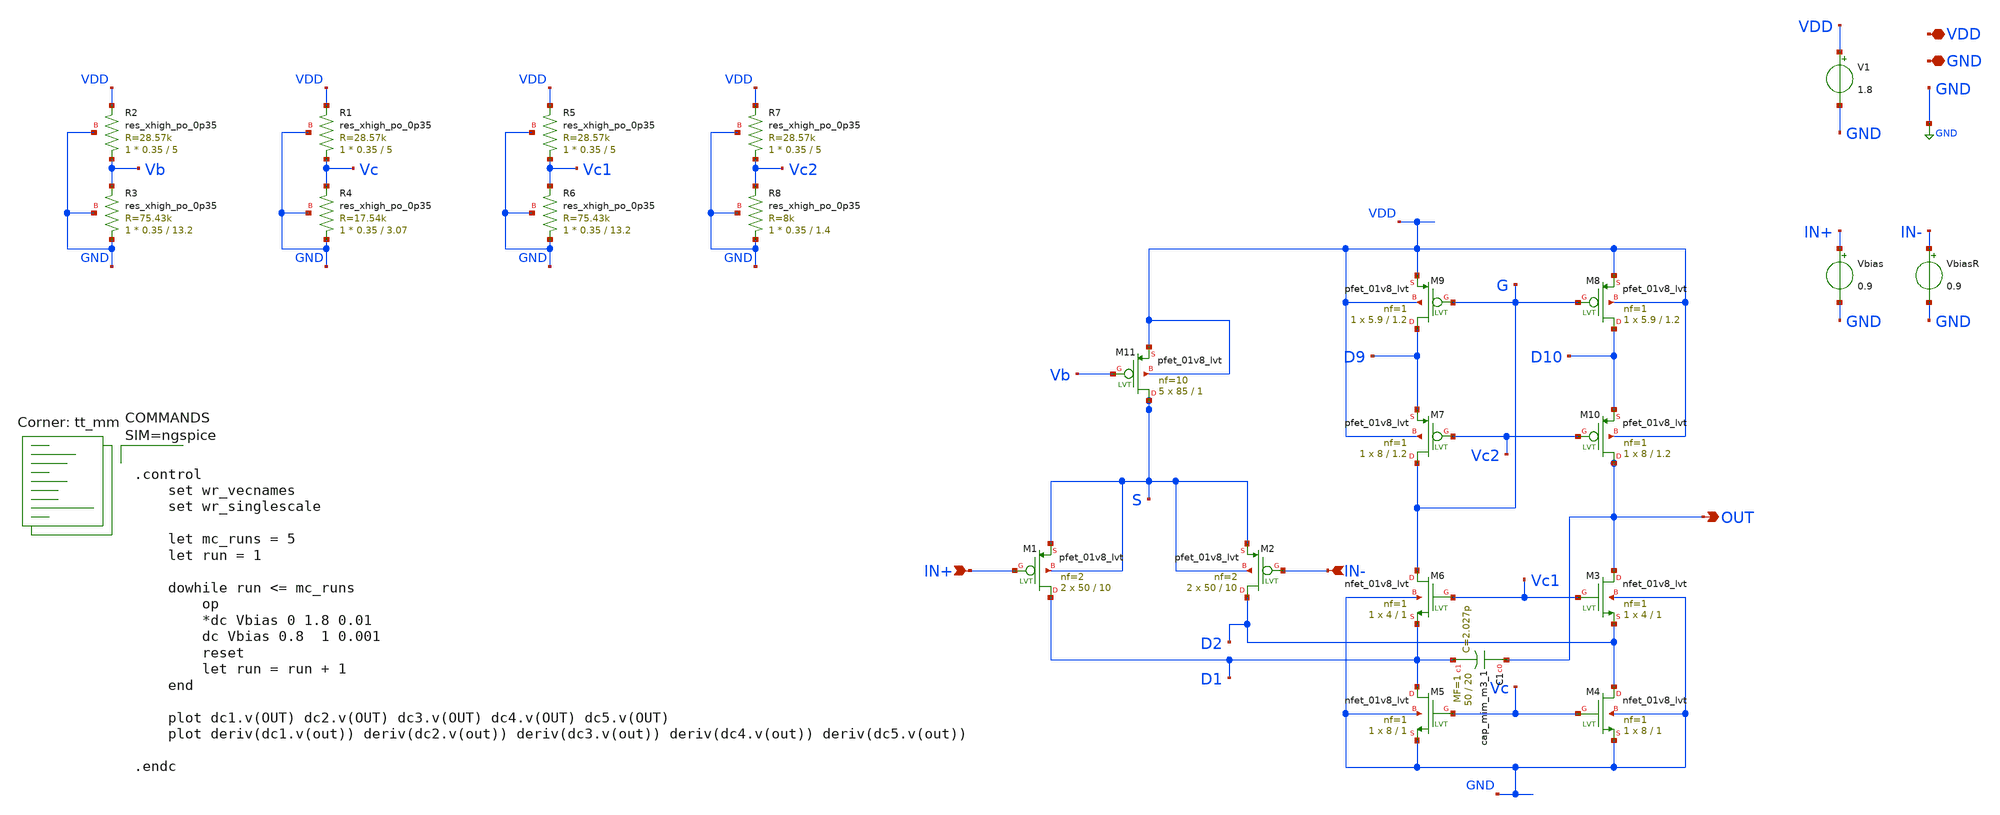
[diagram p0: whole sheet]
** sch_path: xschem/OTA_FoldedCascode1_1_MC.sch
**.subckt OTA_FoldedCascode1_1_MC VDD GND IN+ IN- OUT
*.iopin VDD
*.iopin GND
*.ipin IN+
*.ipin IN-
*.opin OUT
V1 VDD GND 1.8
Vbias IN+ GND 0.9
VbiasR IN- GND 0.9
XM11 S Vb VDD VDD sky130_fd_pr__pfet_01v8_lvt L=1 W=85 nf=10 ad='int((nf+1)/2) * W/nf * 0.29' as='int((nf+2)/2) * W/nf * 0.29'
+ pd='2*int((nf+1)/2) * (W/nf + 0.29)' ps='2*int((nf+2)/2) * (W/nf + 0.29)' nrd='0.29 / W' nrs='0.29 / W'
+ sa=0 sb=0 sd=0 mult=5 m=5
XM1 D1 IN+ S S sky130_fd_pr__pfet_01v8_lvt L=10 W=50 nf=2 ad='int((nf+1)/2) * W/nf * 0.29' as='int((nf+2)/2) * W/nf * 0.29'
+ pd='2*int((nf+1)/2) * (W/nf + 0.29)' ps='2*int((nf+2)/2) * (W/nf + 0.29)' nrd='0.29 / W' nrs='0.29 / W'
+ sa=0 sb=0 sd=0 mult=2 m=2
XM2 D2 IN- S S sky130_fd_pr__pfet_01v8_lvt L=10 W=50 nf=2 ad='int((nf+1)/2) * W/nf * 0.29' as='int((nf+2)/2) * W/nf * 0.29'
+ pd='2*int((nf+1)/2) * (W/nf + 0.29)' ps='2*int((nf+2)/2) * (W/nf + 0.29)' nrd='0.29 / W' nrs='0.29 / W'
+ sa=0 sb=0 sd=0 mult=2 m=2
XM3 OUT Vc1 D2 GND sky130_fd_pr__nfet_01v8_lvt L=1 W=4 nf=1 ad='int((nf+1)/2) * W/nf * 0.29' as='int((nf+2)/2) * W/nf * 0.29'
+ pd='2*int((nf+1)/2) * (W/nf + 0.29)' ps='2*int((nf+2)/2) * (W/nf + 0.29)' nrd='0.29 / W' nrs='0.29 / W'
+ sa=0 sb=0 sd=0 mult=1 m=1
XM4 D2 Vc GND GND sky130_fd_pr__nfet_01v8_lvt L=1 W=8 nf=1 ad='int((nf+1)/2) * W/nf * 0.29' as='int((nf+2)/2) * W/nf * 0.29'
+ pd='2*int((nf+1)/2) * (W/nf + 0.29)' ps='2*int((nf+2)/2) * (W/nf + 0.29)' nrd='0.29 / W' nrs='0.29 / W'
+ sa=0 sb=0 sd=0 mult=1 m=1
XM5 D1 Vc GND GND sky130_fd_pr__nfet_01v8_lvt L=1 W=8 nf=1 ad='int((nf+1)/2) * W/nf * 0.29' as='int((nf+2)/2) * W/nf * 0.29'
+ pd='2*int((nf+1)/2) * (W/nf + 0.29)' ps='2*int((nf+2)/2) * (W/nf + 0.29)' nrd='0.29 / W' nrs='0.29 / W'
+ sa=0 sb=0 sd=0 mult=1 m=1
XM6 G Vc1 D1 GND sky130_fd_pr__nfet_01v8_lvt L=1 W=4 nf=1 ad='int((nf+1)/2) * W/nf * 0.29' as='int((nf+2)/2) * W/nf * 0.29'
+ pd='2*int((nf+1)/2) * (W/nf + 0.29)' ps='2*int((nf+2)/2) * (W/nf + 0.29)' nrd='0.29 / W' nrs='0.29 / W'
+ sa=0 sb=0 sd=0 mult=1 m=1
XR2 Vb VDD GND sky130_fd_pr__res_xhigh_po_0p35 L=5 mult=1 m=1
XR3 GND Vb GND sky130_fd_pr__res_xhigh_po_0p35 L=13.2 mult=1 m=1
XR1 Vc VDD GND sky130_fd_pr__res_xhigh_po_0p35 L=5 mult=1 m=1
XR4 GND Vc GND sky130_fd_pr__res_xhigh_po_0p35 L=3.07 mult=1 m=1
XR5 Vc1 VDD GND sky130_fd_pr__res_xhigh_po_0p35 L=5 mult=1 m=1
XR6 GND Vc1 GND sky130_fd_pr__res_xhigh_po_0p35 L=13.2 mult=1 m=1
XR7 Vc2 VDD GND sky130_fd_pr__res_xhigh_po_0p35 L=5 mult=1 m=1
XR8 GND Vc2 GND sky130_fd_pr__res_xhigh_po_0p35 L=1.4 mult=1 m=1
XM7 G Vc2 D9 VDD sky130_fd_pr__pfet_01v8_lvt L=1.2 W=8 nf=1 ad='int((nf+1)/2) * W/nf * 0.29' as='int((nf+2)/2) * W/nf * 0.29'
+ pd='2*int((nf+1)/2) * (W/nf + 0.29)' ps='2*int((nf+2)/2) * (W/nf + 0.29)' nrd='0.29 / W' nrs='0.29 / W'
+ sa=0 sb=0 sd=0 mult=1 m=1
XM9 D9 G VDD VDD sky130_fd_pr__pfet_01v8_lvt L=1.2 W=5.9 nf=1 ad='int((nf+1)/2) * W/nf * 0.29' as='int((nf+2)/2) * W/nf * 0.29'
+ pd='2*int((nf+1)/2) * (W/nf + 0.29)' ps='2*int((nf+2)/2) * (W/nf + 0.29)' nrd='0.29 / W' nrs='0.29 / W'
+ sa=0 sb=0 sd=0 mult=1 m=1
XM8 D10 G VDD VDD sky130_fd_pr__pfet_01v8_lvt L=1.2 W=5.9 nf=1 ad='int((nf+1)/2) * W/nf * 0.29' as='int((nf+2)/2) * W/nf * 0.29'
+ pd='2*int((nf+1)/2) * (W/nf + 0.29)' ps='2*int((nf+2)/2) * (W/nf + 0.29)' nrd='0.29 / W' nrs='0.29 / W'
+ sa=0 sb=0 sd=0 mult=1 m=1
XM10 OUT Vc2 D10 VDD sky130_fd_pr__pfet_01v8_lvt L=1.2 W=8 nf=1 ad='int((nf+1)/2) * W/nf * 0.29' as='int((nf+2)/2) * W/nf * 0.29'
+ pd='2*int((nf+1)/2) * (W/nf + 0.29)' ps='2*int((nf+2)/2) * (W/nf + 0.29)' nrd='0.29 / W' nrs='0.29 / W'
+ sa=0 sb=0 sd=0 mult=1 m=1
XC1 OUT D1 sky130_fd_pr__cap_mim_m3_1 W=50 L=20 MF=1 m=1
**** begin user architecture code



.control
    set wr_vecnames
    set wr_singlescale

    let mc_runs = 5
    let run = 1

    dowhile run <= mc_runs
        op
        *dc Vbias 0 1.8 0.01
        dc Vbias 0.8  1 0.001
        reset
        let run = run + 1
    end

    plot dc1.v(OUT) dc2.v(OUT) dc3.v(OUT) dc4.v(OUT) dc5.v(OUT)
    plot deriv(dc1.v(out)) deriv(dc2.v(out)) deriv(dc3.v(out)) deriv(dc4.v(out)) deriv(dc5.v(out))

.endc


.lib $::SKYWATER_MODELS/sky130.lib.spice tt_mm
**** end user architecture code
**.ends
.GLOBAL GND
.end
